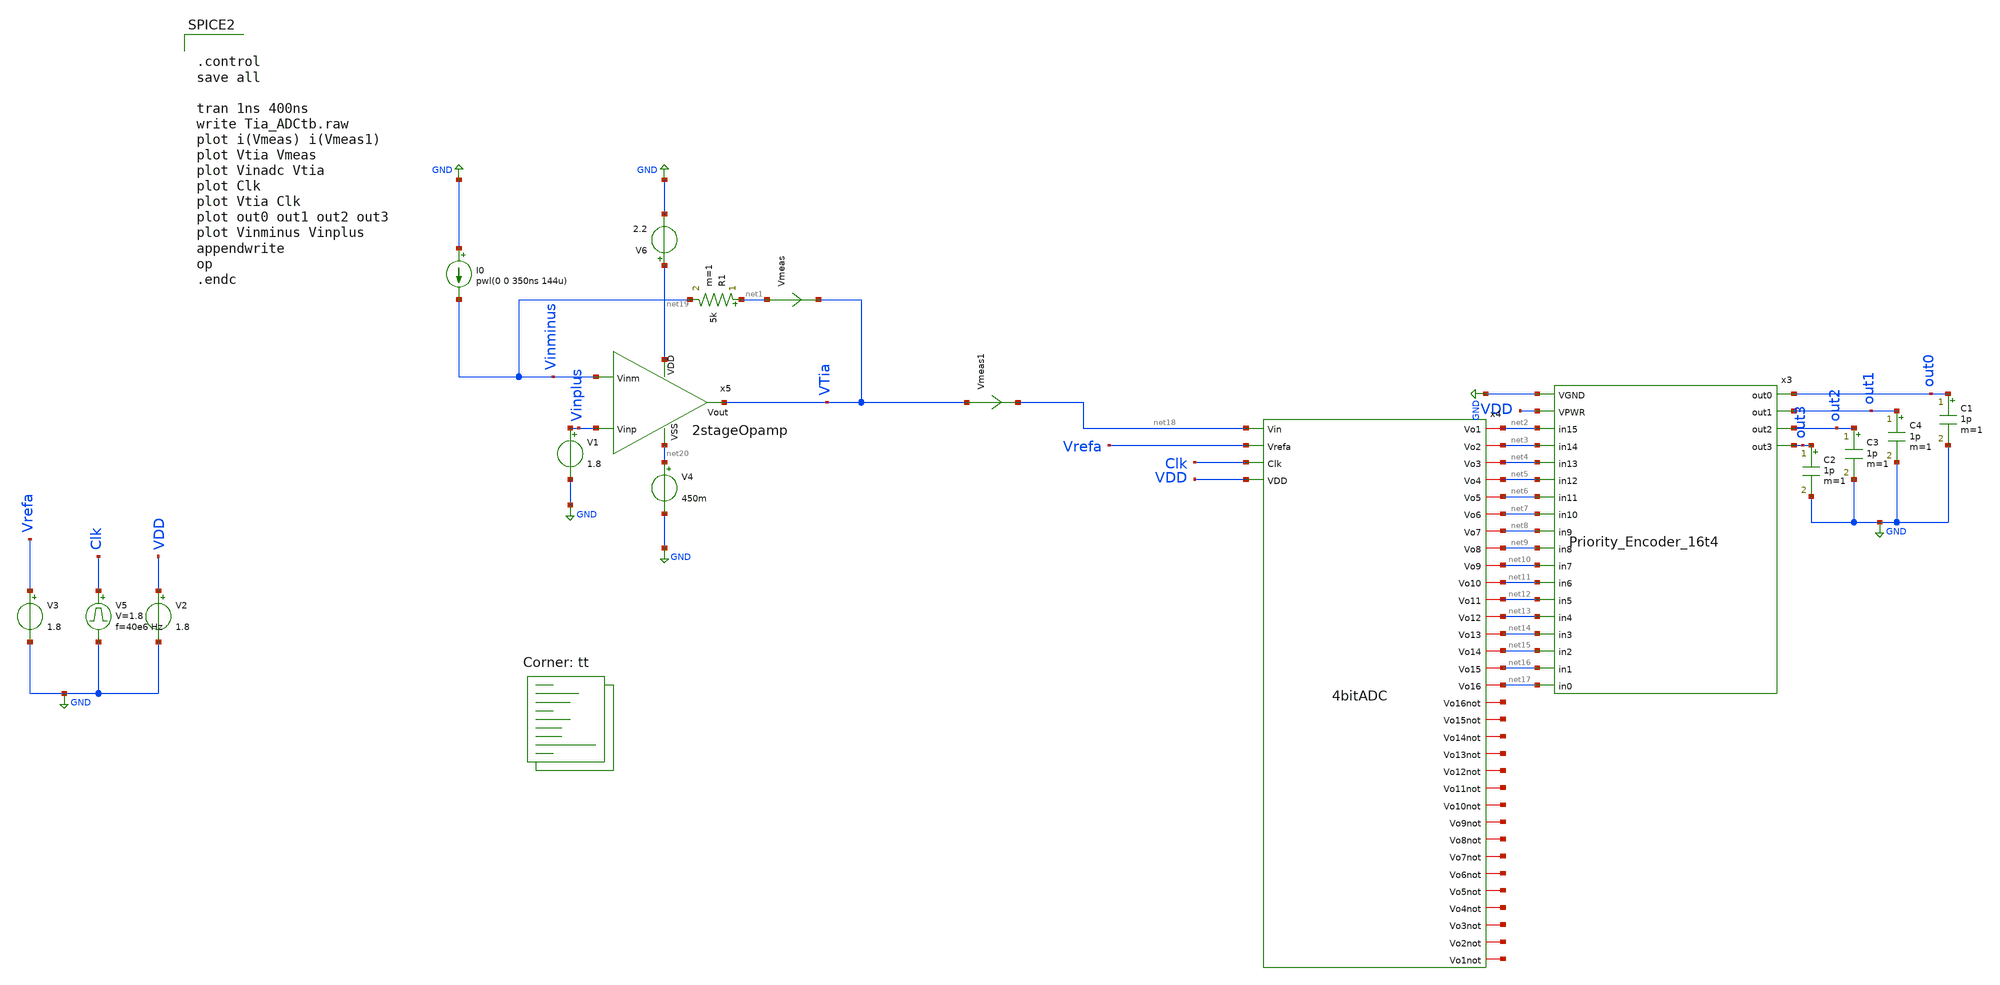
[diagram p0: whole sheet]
** sch_path: Tia_ADCtb.sch
**.subckt Tia_ADCtb
I0 GND Vinminus pwl(0 0 350ns 144u)
R1 net1 Vinminus 5k m=1
V1 Vinplus GND 1.8
Vmeas net1 VTia 0
.save i(vmeas)
V2 VDD GND 1.8
V3 Vrefa GND 1.8
.save i(v3)
V5 Clk GND pulse 0 1.8 '0.495/ 40e6 ' '0.01/40e6 ' '0.01/40e6 ' '0.49/40e6 ' '1/40e6 '
x3 GND VDD net17 net16 net7 net6 net5 net4 net3 net2 net15 net14 net13 net12 net11 net10 net9 net8
+ out0 out1 out2 out3 Priority_Encoder_16t4
x4 net2 net3 net18 net4 Vrefa net5 net6 Clk net7 net8 VDD net9 net10 net11 net12 net13 net14 net15
+ net16 net17 net21 net22 net23 net24 net25 net26 net27 net28 net29 net30 net31 net32 net33 net34 net35
+ net36 4bitADC
C1 out0 GND 1p m=1
C2 out3 GND 1p m=1
C3 out2 GND 1p m=1
C4 out1 GND 1p m=1
x5 net19 Vinminus Vinplus VTia net20 2stageOpamp
Vmeas1 VTia net18 0
.save i(vmeas1)
V4 net20 GND 450m
V6 net19 GND 2.2
**** begin user architecture code
.lib $::SKYWATER_MODELS/sky130.lib.spice tt


.control
save all

tran 1ns 400ns
write Tia_ADCtb.raw
plot i(Vmeas) i(Vmeas1)
plot Vtia Vmeas
plot Vinadc Vtia
plot Clk
plot Vtia Clk
plot out0 out1 out2 out3
plot Vinminus Vinplus
appendwrite
op
.endc



** opencircuitdesign pdks install
.include $::SKYWATER_STDCELLS/sky130_fd_sc_hd.spice


**** end user architecture code
**.ends
.GLOBAL GND
.end
